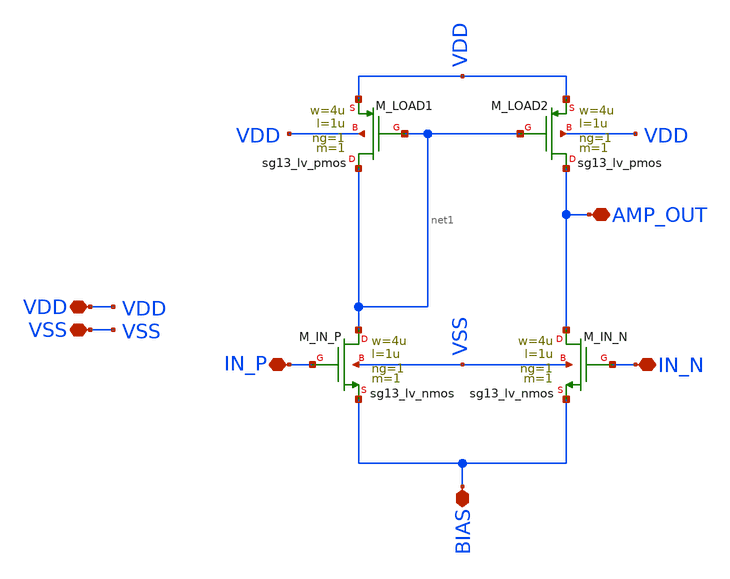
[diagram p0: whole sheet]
** sch_path: xschem/OTA-C.sch
**.subckt OTA-C VDD IN_N IN_P AMP_OUT VSS BIAS
*.iopin VDD
*.iopin IN_N
*.iopin IN_P
*.iopin AMP_OUT
*.iopin VSS
*.iopin BIAS
XM_LOAD1 net1 net1 VDD VDD sg13_lv_pmos w=4u l=1u ng=1 m=1 mm_ok=1
XM_IN_P net1 IN_P BIAS VSS sg13_lv_nmos w=4u l=1u ng=1 m=1 mm_ok=1
XM_IN_N AMP_OUT IN_N BIAS VSS sg13_lv_nmos w=4u l=1u ng=1 m=1 mm_ok=1
XM_LOAD2 AMP_OUT net1 VDD VDD sg13_lv_pmos w=4u l=1u ng=1 m=1 mm_ok=1
**.ends
.end
